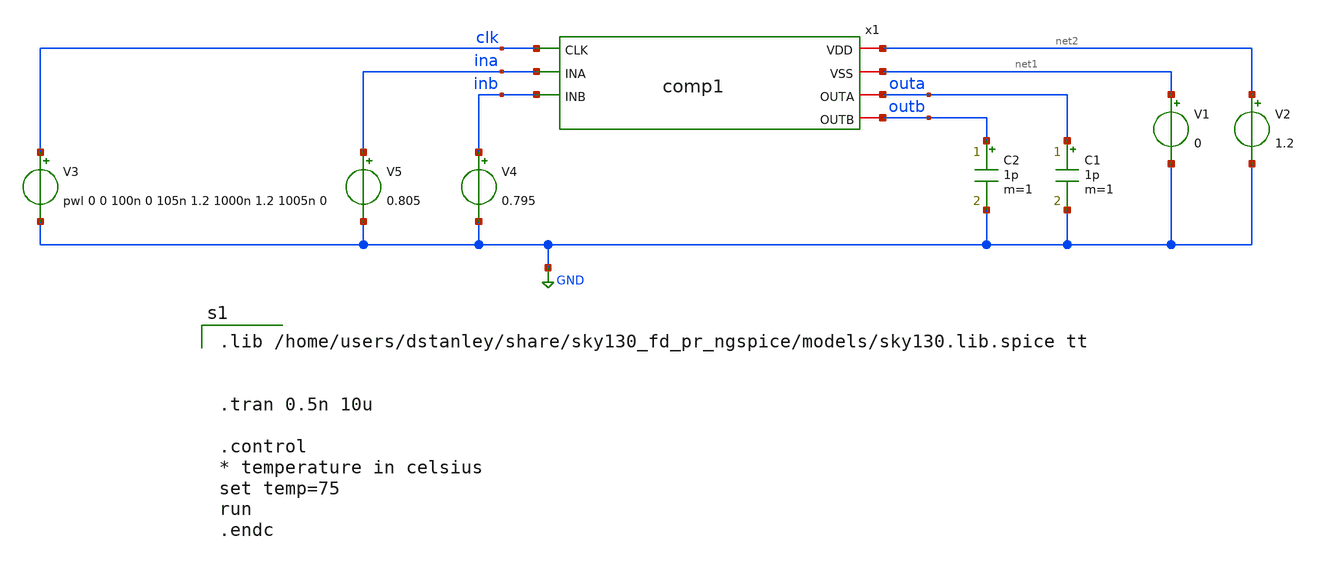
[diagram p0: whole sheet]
** sch_path: comp1_test_temperature.sch
**.subckt comp1_test_temperature
x1 net2 net1 clk ina inb outa outb comp1
V1 net1 GND 0
V2 net2 GND 1.2
C1 outa GND 1p m=1
C2 outb GND 1p m=1
V3 clk GND pwl 0 0 100n 0 105n 1.2 1000n 1.2 1005n 0
V4 inb GND 0.795
V5 ina GND 0.805
**** begin user architecture code

.lib /home/users/dstanley/share/sky130_fd_pr_ngspice/models/sky130.lib.spice tt


.tran 0.5n 10u

.control
* temperature in celsius
set temp=75
run
.endc


**** end user architecture code
**.ends

* expanding   symbol:  /home/users/dstanley/EE272B/xschem_tests/comp1.sym # of pins=7
** sym_path: comp1.sym
** sch_path: comp1.sch
.subckt comp1 VDD VSS CLK INA INB OUTA OUTB
*.iopin VSS
*.iopin VDD
*.iopin OUTB
*.iopin OUTA
*.ipin INB
*.ipin INA
*.ipin CLK
XM1 net2 CLK VSS VSS sky130_fd_pr__nfet_01v8 L=0.15 W=1 nf=1 ad='int((nf+1)/2) * W/nf * 0.29' as='int((nf+2)/2) * W/nf * 0.29'
+ pd='2*int((nf+1)/2) * (W/nf + 0.29)' ps='2*int((nf+2)/2) * (W/nf + 0.29)' nrd='0.29 / W' nrs='0.29 / W'
+ sa=0 sb=0 sd=0 mult=1 m=1
XM2 net1 INA net2 VSS sky130_fd_pr__nfet_01v8 L=0.15 W=1 nf=1 ad='int((nf+1)/2) * W/nf * 0.29' as='int((nf+2)/2) * W/nf * 0.29'
+ pd='2*int((nf+1)/2) * (W/nf + 0.29)' ps='2*int((nf+2)/2) * (W/nf + 0.29)' nrd='0.29 / W' nrs='0.29 / W'
+ sa=0 sb=0 sd=0 mult=1 m=1
XM4 OUTB OUTA net1 VSS sky130_fd_pr__nfet_01v8 L=0.15 W=1 nf=1 ad='int((nf+1)/2) * W/nf * 0.29' as='int((nf+2)/2) * W/nf * 0.29'
+ pd='2*int((nf+1)/2) * (W/nf + 0.29)' ps='2*int((nf+2)/2) * (W/nf + 0.29)' nrd='0.29 / W' nrs='0.29 / W'
+ sa=0 sb=0 sd=0 mult=1 m=1
XM5 OUTB OUTA VDD VDD sky130_fd_pr__pfet_01v8 L=0.15 W=1 nf=1 ad='int((nf+1)/2) * W/nf * 0.29' as='int((nf+2)/2) * W/nf * 0.29'
+ pd='2*int((nf+1)/2) * (W/nf + 0.29)' ps='2*int((nf+2)/2) * (W/nf + 0.29)' nrd='0.29 / W' nrs='0.29 / W'
+ sa=0 sb=0 sd=0 mult=1 m=1
XM6 OUTB CLK VDD VDD sky130_fd_pr__pfet_01v8 L=0.15 W=1 nf=1 ad='int((nf+1)/2) * W/nf * 0.29' as='int((nf+2)/2) * W/nf * 0.29'
+ pd='2*int((nf+1)/2) * (W/nf + 0.29)' ps='2*int((nf+2)/2) * (W/nf + 0.29)' nrd='0.29 / W' nrs='0.29 / W'
+ sa=0 sb=0 sd=0 mult=1 m=1
XM3 net3 INB net2 VSS sky130_fd_pr__nfet_01v8 L=0.15 W=1 nf=1 ad='int((nf+1)/2) * W/nf * 0.29' as='int((nf+2)/2) * W/nf * 0.29'
+ pd='2*int((nf+1)/2) * (W/nf + 0.29)' ps='2*int((nf+2)/2) * (W/nf + 0.29)' nrd='0.29 / W' nrs='0.29 / W'
+ sa=0 sb=0 sd=0 mult=1 m=1
XM7 OUTA OUTB net3 VSS sky130_fd_pr__nfet_01v8 L=0.15 W=1 nf=1 ad='int((nf+1)/2) * W/nf * 0.29' as='int((nf+2)/2) * W/nf * 0.29'
+ pd='2*int((nf+1)/2) * (W/nf + 0.29)' ps='2*int((nf+2)/2) * (W/nf + 0.29)' nrd='0.29 / W' nrs='0.29 / W'
+ sa=0 sb=0 sd=0 mult=1 m=1
XM8 OUTA OUTB VDD VDD sky130_fd_pr__pfet_01v8 L=0.15 W=1 nf=1 ad='int((nf+1)/2) * W/nf * 0.29' as='int((nf+2)/2) * W/nf * 0.29'
+ pd='2*int((nf+1)/2) * (W/nf + 0.29)' ps='2*int((nf+2)/2) * (W/nf + 0.29)' nrd='0.29 / W' nrs='0.29 / W'
+ sa=0 sb=0 sd=0 mult=1 m=1
XM9 OUTA CLK VDD VDD sky130_fd_pr__pfet_01v8 L=0.15 W=1 nf=1 ad='int((nf+1)/2) * W/nf * 0.29' as='int((nf+2)/2) * W/nf * 0.29'
+ pd='2*int((nf+1)/2) * (W/nf + 0.29)' ps='2*int((nf+2)/2) * (W/nf + 0.29)' nrd='0.29 / W' nrs='0.29 / W'
+ sa=0 sb=0 sd=0 mult=1 m=1
.ends

.GLOBAL GND
.end
